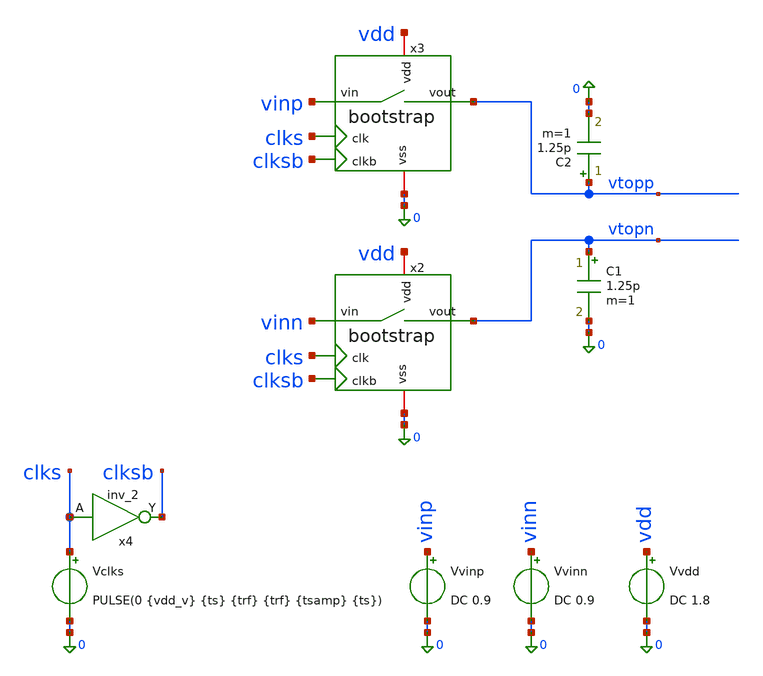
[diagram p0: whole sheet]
** sch_path: xschem/sar-adc_tb/tb5_mc.sch
.lib $::SKYWATER_MODELS/sky130.lib.spice tt_mm
.include $::SKYWATER_STDCELLS/sky130_fd_sc_hd.spice

**.subckt tb5_mc
x2 clks clksb vinn vtopn vdd 0 bootstrap
x3 clks clksb vinp vtopp vdd 0 bootstrap
C1 vtopn 0 1.25p m=1
C2 vtopp 0 1.25p m=1
Vclks clks 0 PULSE(0 {vdd_v} {ts} {trf} {trf} {tsamp} {ts})
x4 clks 0 0 dvdd dvdd clksb sky130_fd_sc_hd__inv_2
Vvinp vinp 0 DC 0.9
Vvinn vinn 0 DC 0.9
Vvdd vdd 0 DC 1.8
**** begin user architecture code


.param tcomp_d = 'ts + 20e-9'    $ strobe 5 ns setelah switch membuka
.param tcomp_w = 25e-9
.param vdd_v   = 1.8
.param fs      = 10e6
.param ts      = '1/fs'          $ 100 ns
.param tsamp   = 15e-9           $ jendela track
.param trf     = 100e-12         $ rise/fall clock (buffer riil, bukan 1 ps)




.control
  echo ''
  echo '=== TB5  Monte Carlo mismatch pasangan bootstrap ================'
  echo 'Corner tt_mm. Variabel `run` adalah SEED yang dibaca model'
  echo 'sky130; ia harus di-set SEBELUM tiap analisis dan didahului'
  echo '`reset` supaya netlist dievaluasi ulang dengan seed baru.'
  echo ''

  let r = 0
  dowhile r < 100
    reset
    let run = r
    tran 20p 250n
    setplot $curplot
    meas tran op FIND v(vtopp) AT=195n
    meas tran on FIND v(vtopn) AT=195n
    let off_uv = (op - on)*1e6
    echo 'MC $&r $&off_uv'
    let r = r + 1
  end
  echo '=== akhir MC ===================================================='
  echo ''
.endc


**** end user architecture code
**.ends

* expanding   symbol:  bootstrap.sym # of pins=6
** sym_path: xschem/sar-adc/bootstrap.sym
** sch_path: xschem/sar-adc/bootstrap.sch
.subckt bootstrap clk clkb vin vout vdd vss
*.ipin clk
*.ipin clkb
*.ipin vin
*.opin vout
*.iopin vdd
*.iopin vss
XMswitch vin vgate vout vss sky130_fd_pr__nfet_01v8 L=0.15 W=2 nf=1 ad='int((1 + 1)/2) * 2 / 1 * 0.29'
+ as='int((1 + 2)/2) * 2 / 1 * 0.29' pd='2*int((1 + 1)/2) * (2 / 1 + 0.29)' ps='2*int((1 + 2)/2) * (2 / 1 + 0.29)'
+ nrd='0.29 / 2 ' nrs='0.29 / 2 ' sa=0 sb=0 sd=0 mult=1 m=1
XMdisbot cbot vgate vin vss sky130_fd_pr__nfet_01v8 L=0.15 W=1 nf=1 ad='int((1 + 1)/2) * 1 / 1 * 0.29'
+ as='int((1 + 2)/2) * 1 / 1 * 0.29' pd='2*int((1 + 1)/2) * (1 / 1 + 0.29)' ps='2*int((1 + 2)/2) * (1 / 1 + 0.29)'
+ nrd='0.29 / 1 ' nrs='0.29 / 1 ' sa=0 sb=0 sd=0 mult=1 m=1
XCboot ctop cbot sky130_fd_pr__cap_mim_m3_1 W=10 L=10 MF=1 m=1
XMdistop vgate vgdistop ctop ctop sky130_fd_pr__pfet_01v8 L=0.15 W=1 nf=1 ad='int((1 + 1)/2) * 1 / 1 * 0.29'
+ as='int((1 + 2)/2) * 1 / 1 * 0.29' pd='2*int((1 + 1)/2) * (1 / 1 + 0.29)' ps='2*int((1 + 2)/2) * (1 / 1 + 0.29)'
+ nrd='0.29 / 1 ' nrs='0.29 / 1 ' sa=0 sb=0 sd=0 mult=1 m=1
XMchtop ctop vgate vdd ctop sky130_fd_pr__pfet_01v8 L=0.15 W=1 nf=1 ad='int((1 + 1)/2) * 1 / 1 * 0.29'
+ as='int((1 + 2)/2) * 1 / 1 * 0.29' pd='2*int((1 + 1)/2) * (1 / 1 + 0.29)' ps='2*int((1 + 2)/2) * (1 / 1 + 0.29)'
+ nrd='0.29 / 1 ' nrs='0.29 / 1 ' sa=0 sb=0 sd=0 mult=1 m=1
XMdistopdrv vgdistop vgate cbot vss sky130_fd_pr__nfet_01v8 L=0.15 W=0.5 nf=1 ad='int((1 + 1)/2) * 0.5 / 1 * 0.29'
+ as='int((1 + 2)/2) * 0.5 / 1 * 0.29' pd='2*int((1 + 1)/2) * (0.5 / 1 + 0.29)' ps='2*int((1 + 2)/2) * (0.5 / 1 + 0.29)'
+ nrd='0.29 / 0.5 ' nrs='0.29 / 0.5 ' sa=0 sb=0 sd=0 mult=1 m=1
XMchtopdrv2 vschtopdrv1 clkb vss vss sky130_fd_pr__nfet_01v8 L=0.15 W=1 nf=1 ad='int((1 + 1)/2) * 1 / 1 * 0.29'
+ as='int((1 + 2)/2) * 1 / 1 * 0.29' pd='2*int((1 + 1)/2) * (1 / 1 + 0.29)' ps='2*int((1 + 2)/2) * (1 / 1 + 0.29)'
+ nrd='0.29 / 1 ' nrs='0.29 / 1 ' sa=0 sb=0 sd=0 mult=1 m=1
XMchbot cbot clkb vss vss sky130_fd_pr__nfet_01v8 L=0.15 W=1 nf=1 ad='int((1 + 1)/2) * 1 / 1 * 0.29'
+ as='int((1 + 2)/2) * 1 / 1 * 0.29' pd='2*int((1 + 1)/2) * (1 / 1 + 0.29)' ps='2*int((1 + 2)/2) * (1 / 1 + 0.29)'
+ nrd='0.29 / 1 ' nrs='0.29 / 1 ' sa=0 sb=0 sd=0 mult=1 m=1
XM1 vgdistop clk vdd vdd sky130_fd_pr__pfet_01v8 L=0.15 W=1 nf=1 ad='int((1 + 1)/2) * 1 / 1 * 0.29' as='int((1 + 2)/2) * 1 / 1 * 0.29'
+ pd='2*int((1 + 1)/2) * (1 / 1 + 0.29)' ps='2*int((1 + 2)/2) * (1 / 1 + 0.29)' nrd='0.29 / 1 ' nrs='0.29 / 1 '
+ sa=0 sb=0 sd=0 mult=1 m=1
XM2 vgdistop clk cbot vss sky130_fd_pr__nfet_01v8 L=0.15 W=0.5 nf=1 ad='int((1 + 1)/2) * 0.5 / 1 * 0.29'
+ as='int((1 + 2)/2) * 0.5 / 1 * 0.29' pd='2*int((1 + 1)/2) * (0.5 / 1 + 0.29)' ps='2*int((1 + 2)/2) * (0.5 / 1 + 0.29)'
+ nrd='0.29 / 0.5 ' nrs='0.29 / 0.5 ' sa=0 sb=0 sd=0 mult=1 m=1
XXMchtopdrv1 vgate vdd vschtopdrv1 vss sky130_fd_pr__nfet_g5v0d10v5 L=0.5 W=3 nf=1 ad='int((1 + 1)/2) * 3 / 1 * 0.29'
+ as='int((1 + 2)/2) * 3 / 1 * 0.29' pd='2*int((1 + 1)/2) * (3 / 1 + 0.29)' ps='2*int((1 + 2)/2) * (3 / 1 + 0.29)'
+ nrd='0.29 / 3 ' nrs='0.29 / 3 ' sa=0 sb=0 sd=0 mult=1 m=1
.ends

.end
